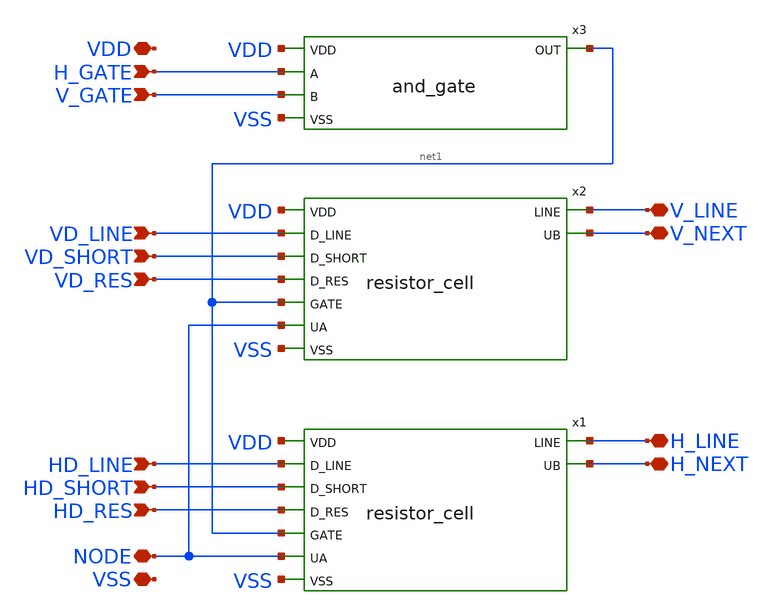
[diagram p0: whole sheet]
** sch_path: xschem/grid_cell.sch
**.subckt grid_cell VSS H_NEXT VDD NODE HD_RES HD_SHORT HD_LINE VD_RES VD_SHORT VD_LINE H_GATE
*+ V_GATE H_LINE V_NEXT V_LINE
*.iopin VSS
*.iopin H_NEXT
*.iopin VDD
*.iopin NODE
*.ipin HD_RES
*.ipin HD_SHORT
*.ipin HD_LINE
*.ipin VD_RES
*.ipin VD_SHORT
*.ipin VD_LINE
*.ipin H_GATE
*.ipin V_GATE
*.iopin H_LINE
*.iopin V_NEXT
*.iopin V_LINE
x1 VDD H_LINE HD_LINE HD_SHORT H_NEXT HD_RES net1 NODE VSS resistor_cell
x2 VDD V_LINE VD_LINE VD_SHORT V_NEXT VD_RES net1 NODE VSS resistor_cell
x3 VDD net1 H_GATE V_GATE VSS and_gate
**.ends
.end
